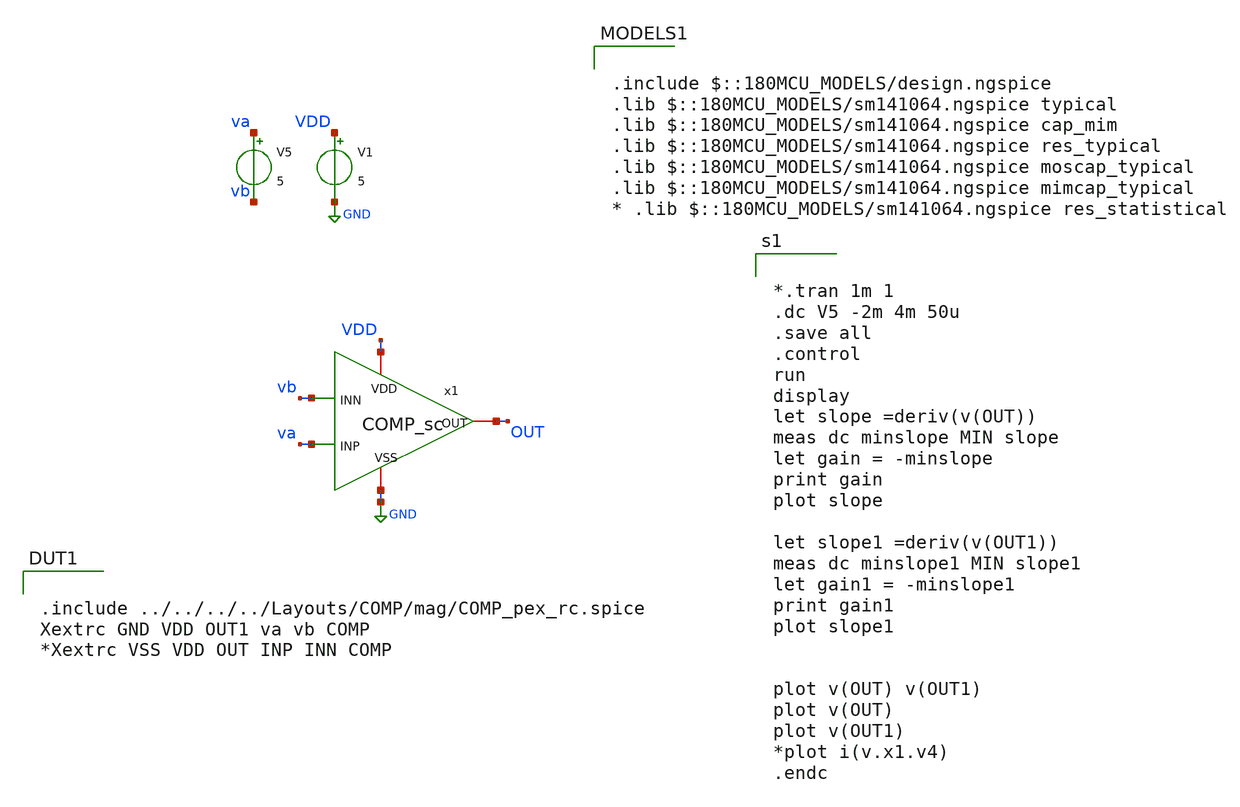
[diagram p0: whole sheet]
** sch_path: FINAL/XSCHEM/TEST/test_comp_dc.sch
**.subckt test_comp_dc
V1 VDD GND 5
V5 va vb 5
x1 VDD vb OUT va GND COMP_sc
**** begin user architecture code


*.tran 1m 1
.dc V5 -2m 4m 50u
.save all
.control
run
display
let slope =deriv(v(OUT))
meas dc minslope MIN slope
let gain = -minslope
print gain
plot slope

let slope1 =deriv(v(OUT1))
meas dc minslope1 MIN slope1
let gain1 = -minslope1
print gain1
plot slope1


plot v(OUT) v(OUT1)
plot v(OUT)
plot v(OUT1)
*plot i(v.x1.v4)
.endc



.include $::180MCU_MODELS/design.ngspice
.lib $::180MCU_MODELS/sm141064.ngspice typical
.lib $::180MCU_MODELS/sm141064.ngspice cap_mim
.lib $::180MCU_MODELS/sm141064.ngspice res_typical
.lib $::180MCU_MODELS/sm141064.ngspice moscap_typical
.lib $::180MCU_MODELS/sm141064.ngspice mimcap_typical
* .lib $::180MCU_MODELS/sm141064.ngspice res_statistical


.include ../../../../Layouts/COMP/mag/COMP_pex_rc.spice
Xextrc GND VDD OUT1 va vb COMP
*Xextrc VSS VDD OUT INP INN COMP


**** end user architecture code
**.ends
.GLOBAL GND
.end
